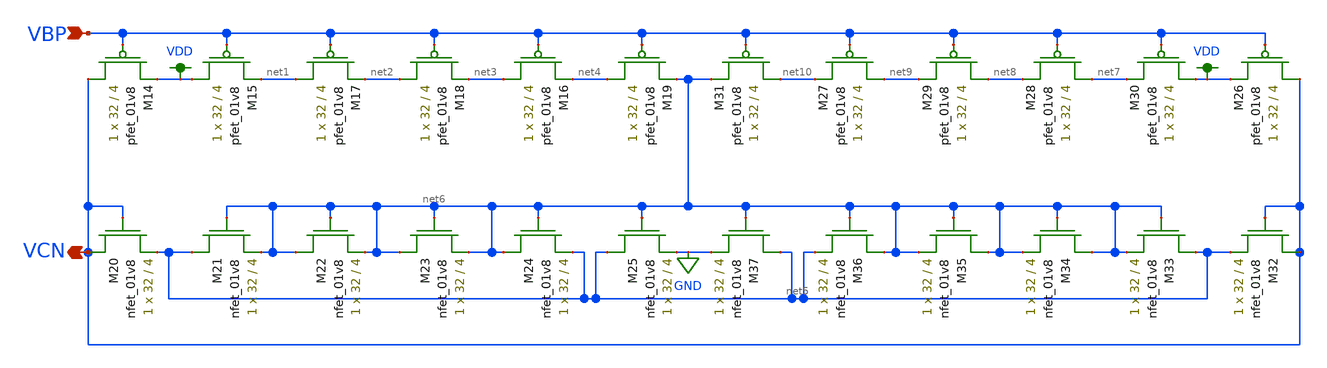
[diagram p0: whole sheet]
** sch_path: schemas/LDS_VCN_GEN.sch
**.subckt LDS_VCN_GEN VBP VCN
*.ipin VBP
*.opin VCN
XM14 VCN VBP VDD VDD sky130_fd_pr__pfet_01v8 L=4 W=32 nf=1 ad='int((nf+1)/2) * W/nf * 0.29' as='int((nf+2)/2) * W/nf * 0.29'
+ pd='2*int((nf+1)/2) * (W/nf + 0.29)' ps='2*int((nf+2)/2) * (W/nf + 0.29)' nrd='0.29 / W' nrs='0.29 / W'
+ sa=0 sb=0 sd=0 mult=1 m=1
XM16 net3 VBP net4 VDD sky130_fd_pr__pfet_01v8 L=4 W=32 nf=1 ad='int((nf+1)/2) * W/nf * 0.29' as='int((nf+2)/2) * W/nf * 0.29'
+ pd='2*int((nf+1)/2) * (W/nf + 0.29)' ps='2*int((nf+2)/2) * (W/nf + 0.29)' nrd='0.29 / W' nrs='0.29 / W'
+ sa=0 sb=0 sd=0 mult=1 m=1
XM17 net1 VBP net2 VDD sky130_fd_pr__pfet_01v8 L=4 W=32 nf=1 ad='int((nf+1)/2) * W/nf * 0.29' as='int((nf+2)/2) * W/nf * 0.29'
+ pd='2*int((nf+1)/2) * (W/nf + 0.29)' ps='2*int((nf+2)/2) * (W/nf + 0.29)' nrd='0.29 / W' nrs='0.29 / W'
+ sa=0 sb=0 sd=0 mult=1 m=1
XM18 net2 VBP net3 VDD sky130_fd_pr__pfet_01v8 L=4 W=32 nf=1 ad='int((nf+1)/2) * W/nf * 0.29' as='int((nf+2)/2) * W/nf * 0.29'
+ pd='2*int((nf+1)/2) * (W/nf + 0.29)' ps='2*int((nf+2)/2) * (W/nf + 0.29)' nrd='0.29 / W' nrs='0.29 / W'
+ sa=0 sb=0 sd=0 mult=1 m=1
XM15 VDD VBP net1 VDD sky130_fd_pr__pfet_01v8 L=4 W=32 nf=1 ad='int((nf+1)/2) * W/nf * 0.29' as='int((nf+2)/2) * W/nf * 0.29'
+ pd='2*int((nf+1)/2) * (W/nf + 0.29)' ps='2*int((nf+2)/2) * (W/nf + 0.29)' nrd='0.29 / W' nrs='0.29 / W'
+ sa=0 sb=0 sd=0 mult=1 m=1
XM19 net4 VBP net6 VDD sky130_fd_pr__pfet_01v8 L=4 W=32 nf=1 ad='int((nf+1)/2) * W/nf * 0.29' as='int((nf+2)/2) * W/nf * 0.29'
+ pd='2*int((nf+1)/2) * (W/nf + 0.29)' ps='2*int((nf+2)/2) * (W/nf + 0.29)' nrd='0.29 / W' nrs='0.29 / W'
+ sa=0 sb=0 sd=0 mult=1 m=1
XM20 VCN VCN net5 GND sky130_fd_pr__nfet_01v8 L=4 W=32 nf=1 ad='int((nf+1)/2) * W/nf * 0.29' as='int((nf+2)/2) * W/nf * 0.29'
+ pd='2*int((nf+1)/2) * (W/nf + 0.29)' ps='2*int((nf+2)/2) * (W/nf + 0.29)' nrd='0.29 / W' nrs='0.29 / W'
+ sa=0 sb=0 sd=0 mult=1 m=1
XM21 net5 net6 net6 GND sky130_fd_pr__nfet_01v8 L=4 W=32 nf=1 ad='int((nf+1)/2) * W/nf * 0.29' as='int((nf+2)/2) * W/nf * 0.29'
+ pd='2*int((nf+1)/2) * (W/nf + 0.29)' ps='2*int((nf+2)/2) * (W/nf + 0.29)' nrd='0.29 / W' nrs='0.29 / W'
+ sa=0 sb=0 sd=0 mult=1 m=1
XM22 net6 net6 net6 GND sky130_fd_pr__nfet_01v8 L=4 W=32 nf=1 ad='int((nf+1)/2) * W/nf * 0.29' as='int((nf+2)/2) * W/nf * 0.29'
+ pd='2*int((nf+1)/2) * (W/nf + 0.29)' ps='2*int((nf+2)/2) * (W/nf + 0.29)' nrd='0.29 / W' nrs='0.29 / W'
+ sa=0 sb=0 sd=0 mult=1 m=1
XM23 net6 net6 net6 GND sky130_fd_pr__nfet_01v8 L=4 W=32 nf=1 ad='int((nf+1)/2) * W/nf * 0.29' as='int((nf+2)/2) * W/nf * 0.29'
+ pd='2*int((nf+1)/2) * (W/nf + 0.29)' ps='2*int((nf+2)/2) * (W/nf + 0.29)' nrd='0.29 / W' nrs='0.29 / W'
+ sa=0 sb=0 sd=0 mult=1 m=1
XM24 net6 net6 net5 GND sky130_fd_pr__nfet_01v8 L=4 W=32 nf=1 ad='int((nf+1)/2) * W/nf * 0.29' as='int((nf+2)/2) * W/nf * 0.29'
+ pd='2*int((nf+1)/2) * (W/nf + 0.29)' ps='2*int((nf+2)/2) * (W/nf + 0.29)' nrd='0.29 / W' nrs='0.29 / W'
+ sa=0 sb=0 sd=0 mult=1 m=1
XM25 net5 net6 GND GND sky130_fd_pr__nfet_01v8 L=4 W=32 nf=1 ad='int((nf+1)/2) * W/nf * 0.29' as='int((nf+2)/2) * W/nf * 0.29'
+ pd='2*int((nf+1)/2) * (W/nf + 0.29)' ps='2*int((nf+2)/2) * (W/nf + 0.29)' nrd='0.29 / W' nrs='0.29 / W'
+ sa=0 sb=0 sd=0 mult=1 m=1
XM26 VCN VBP VDD VDD sky130_fd_pr__pfet_01v8 L=4 W=32 nf=1 ad='int((nf+1)/2) * W/nf * 0.29' as='int((nf+2)/2) * W/nf * 0.29'
+ pd='2*int((nf+1)/2) * (W/nf + 0.29)' ps='2*int((nf+2)/2) * (W/nf + 0.29)' nrd='0.29 / W' nrs='0.29 / W'
+ sa=0 sb=0 sd=0 mult=1 m=1
XM27 net9 VBP net10 VDD sky130_fd_pr__pfet_01v8 L=4 W=32 nf=1 ad='int((nf+1)/2) * W/nf * 0.29' as='int((nf+2)/2) * W/nf * 0.29'
+ pd='2*int((nf+1)/2) * (W/nf + 0.29)' ps='2*int((nf+2)/2) * (W/nf + 0.29)' nrd='0.29 / W' nrs='0.29 / W'
+ sa=0 sb=0 sd=0 mult=1 m=1
XM28 net7 VBP net8 VDD sky130_fd_pr__pfet_01v8 L=4 W=32 nf=1 ad='int((nf+1)/2) * W/nf * 0.29' as='int((nf+2)/2) * W/nf * 0.29'
+ pd='2*int((nf+1)/2) * (W/nf + 0.29)' ps='2*int((nf+2)/2) * (W/nf + 0.29)' nrd='0.29 / W' nrs='0.29 / W'
+ sa=0 sb=0 sd=0 mult=1 m=1
XM29 net8 VBP net9 VDD sky130_fd_pr__pfet_01v8 L=4 W=32 nf=1 ad='int((nf+1)/2) * W/nf * 0.29' as='int((nf+2)/2) * W/nf * 0.29'
+ pd='2*int((nf+1)/2) * (W/nf + 0.29)' ps='2*int((nf+2)/2) * (W/nf + 0.29)' nrd='0.29 / W' nrs='0.29 / W'
+ sa=0 sb=0 sd=0 mult=1 m=1
XM30 VDD VBP net7 VDD sky130_fd_pr__pfet_01v8 L=4 W=32 nf=1 ad='int((nf+1)/2) * W/nf * 0.29' as='int((nf+2)/2) * W/nf * 0.29'
+ pd='2*int((nf+1)/2) * (W/nf + 0.29)' ps='2*int((nf+2)/2) * (W/nf + 0.29)' nrd='0.29 / W' nrs='0.29 / W'
+ sa=0 sb=0 sd=0 mult=1 m=1
XM31 net10 VBP net6 VDD sky130_fd_pr__pfet_01v8 L=4 W=32 nf=1 ad='int((nf+1)/2) * W/nf * 0.29' as='int((nf+2)/2) * W/nf * 0.29'
+ pd='2*int((nf+1)/2) * (W/nf + 0.29)' ps='2*int((nf+2)/2) * (W/nf + 0.29)' nrd='0.29 / W' nrs='0.29 / W'
+ sa=0 sb=0 sd=0 mult=1 m=1
XM32 VCN VCN net5 GND sky130_fd_pr__nfet_01v8 L=4 W=32 nf=1 ad='int((nf+1)/2) * W/nf * 0.29' as='int((nf+2)/2) * W/nf * 0.29'
+ pd='2*int((nf+1)/2) * (W/nf + 0.29)' ps='2*int((nf+2)/2) * (W/nf + 0.29)' nrd='0.29 / W' nrs='0.29 / W'
+ sa=0 sb=0 sd=0 mult=1 m=1
XM33 net5 net6 net6 GND sky130_fd_pr__nfet_01v8 L=4 W=32 nf=1 ad='int((nf+1)/2) * W/nf * 0.29' as='int((nf+2)/2) * W/nf * 0.29'
+ pd='2*int((nf+1)/2) * (W/nf + 0.29)' ps='2*int((nf+2)/2) * (W/nf + 0.29)' nrd='0.29 / W' nrs='0.29 / W'
+ sa=0 sb=0 sd=0 mult=1 m=1
XM34 net6 net6 net6 GND sky130_fd_pr__nfet_01v8 L=4 W=32 nf=1 ad='int((nf+1)/2) * W/nf * 0.29' as='int((nf+2)/2) * W/nf * 0.29'
+ pd='2*int((nf+1)/2) * (W/nf + 0.29)' ps='2*int((nf+2)/2) * (W/nf + 0.29)' nrd='0.29 / W' nrs='0.29 / W'
+ sa=0 sb=0 sd=0 mult=1 m=1
XM35 net6 net6 net6 GND sky130_fd_pr__nfet_01v8 L=4 W=32 nf=1 ad='int((nf+1)/2) * W/nf * 0.29' as='int((nf+2)/2) * W/nf * 0.29'
+ pd='2*int((nf+1)/2) * (W/nf + 0.29)' ps='2*int((nf+2)/2) * (W/nf + 0.29)' nrd='0.29 / W' nrs='0.29 / W'
+ sa=0 sb=0 sd=0 mult=1 m=1
XM36 net6 net6 net5 GND sky130_fd_pr__nfet_01v8 L=4 W=32 nf=1 ad='int((nf+1)/2) * W/nf * 0.29' as='int((nf+2)/2) * W/nf * 0.29'
+ pd='2*int((nf+1)/2) * (W/nf + 0.29)' ps='2*int((nf+2)/2) * (W/nf + 0.29)' nrd='0.29 / W' nrs='0.29 / W'
+ sa=0 sb=0 sd=0 mult=1 m=1
XM37 net5 net6 GND GND sky130_fd_pr__nfet_01v8 L=4 W=32 nf=1 ad='int((nf+1)/2) * W/nf * 0.29' as='int((nf+2)/2) * W/nf * 0.29'
+ pd='2*int((nf+1)/2) * (W/nf + 0.29)' ps='2*int((nf+2)/2) * (W/nf + 0.29)' nrd='0.29 / W' nrs='0.29 / W'
+ sa=0 sb=0 sd=0 mult=1 m=1
**.ends
.GLOBAL VDD
.GLOBAL GND
.end
